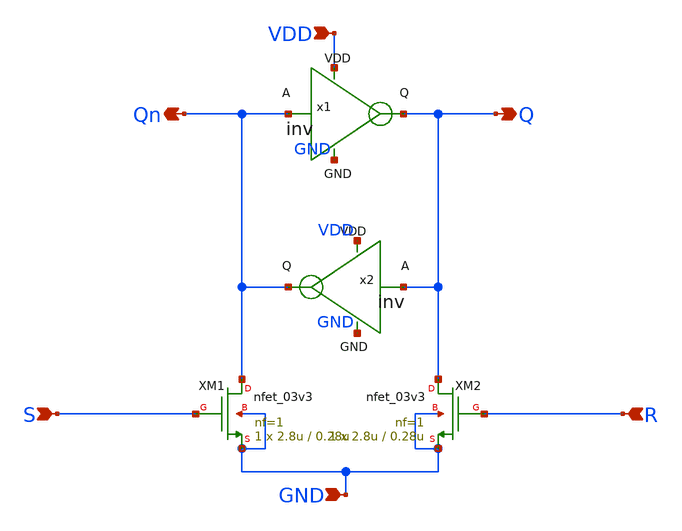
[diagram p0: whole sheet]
** sch_path: latch/new/latch_new.sch
**.subckt latch_new Q Qn GND VDD S R
*.opin Q
*.opin Qn
*.ipin GND
*.ipin VDD
*.ipin S
*.ipin R
x1 VDD Qn Q GND inv
x2 VDD Q Qn GND inv
XM1 Qn S GND GND nfet_03v3 L=0.28u W=2.8u nf=1 ad='int((nf+1)/2) * W/nf * 0.18u' as='int((nf+2)/2) * W/nf * 0.18u'
+ pd='2*int((nf+1)/2) * (W/nf + 0.18u)' ps='2*int((nf+2)/2) * (W/nf + 0.18u)' nrd='0.18u / W' nrs='0.18u / W'
+ sa=0 sb=0 sd=0 m=1
XM2 Q R GND GND nfet_03v3 L=0.28u W=2.8u nf=1 ad='int((nf+1)/2) * W/nf * 0.18u' as='int((nf+2)/2) * W/nf * 0.18u'
+ pd='2*int((nf+1)/2) * (W/nf + 0.18u)' ps='2*int((nf+2)/2) * (W/nf + 0.18u)' nrd='0.18u / W' nrs='0.18u / W'
+ sa=0 sb=0 sd=0 m=1
**.ends

* expanding   symbol:  inverter/inv.sym # of pins=4
** sym_path: review/0407/inverter/inv.sym
** sch_path: review/0407/inverter/inv.sch
.subckt inv VDD A Q GND
*.ipin A
*.opin Q
*.iopin VDD
*.iopin GND
XM1 Q A VDD VDD pfet_03v3 L=0.28u W=2.8u nf=1 ad='int((nf+1)/2) * W/nf * 0.18u' as='int((nf+2)/2) * W/nf * 0.18u'
+ pd='2*int((nf+1)/2) * (W/nf + 0.18u)' ps='2*int((nf+2)/2) * (W/nf + 0.18u)' nrd='0.18u / W' nrs='0.18u / W'
+ sa=0 sb=0 sd=0 m=1
XM2 Q A GND GND nfet_03v3 L=0.28u W=2.8u nf=1 ad='int((nf+1)/2) * W/nf * 0.18u' as='int((nf+2)/2) * W/nf * 0.18u'
+ pd='2*int((nf+1)/2) * (W/nf + 0.18u)' ps='2*int((nf+2)/2) * (W/nf + 0.18u)' nrd='0.18u / W' nrs='0.18u / W'
+ sa=0 sb=0 sd=0 m=1
.ends

.end
